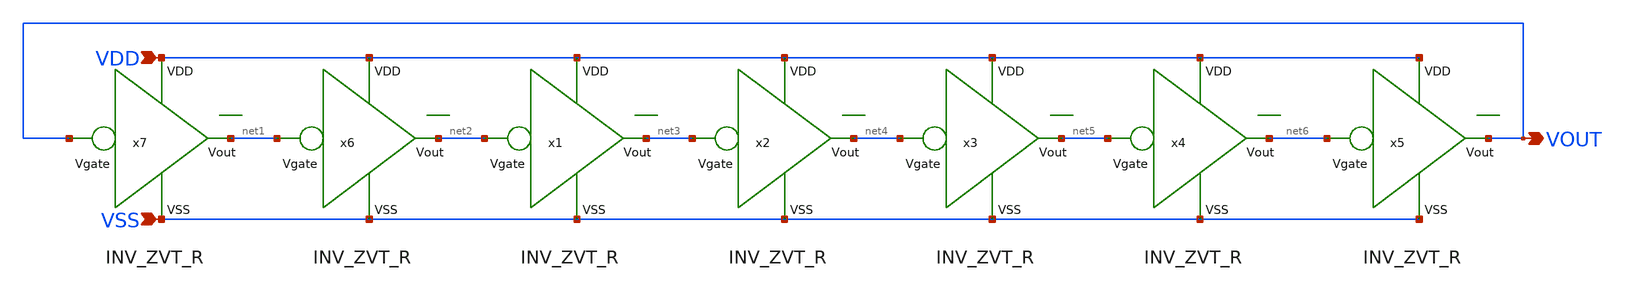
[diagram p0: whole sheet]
** sch_path: design/THESIS_EXP_RO_INVERTER_SKY130A/OSC_ZVT.sch
**.subckt OSC_ZVT VDD VSS VOUT
*.ipin VDD
*.ipin VSS
*.opin VOUT
x1 VDD net3 net2 VSS INV_ZVT_R
x2 VDD net4 net3 VSS INV_ZVT_R
x3 VDD net5 net4 VSS INV_ZVT_R
x4 VDD net6 net5 VSS INV_ZVT_R
x5 VDD VOUT net6 VSS INV_ZVT_R
x6 VDD net2 net1 VSS INV_ZVT_R
x7 VDD net1 VOUT VSS INV_ZVT_R
**.ends

* expanding   symbol:  THESIS_EXP_RO_INVERTER_SKY130A/INV_ZVT_R.sym # of pins=4
** sym_path: design/THESIS_EXP_RO_INVERTER_SKY130A/INV_ZVT_R.sym
** sch_path: design/THESIS_EXP_RO_INVERTER_SKY130A/INV_ZVT_R.sch
.subckt INV_ZVT_R VDD Vout Vgate VSS
*.ipin VDD
*.ipin VSS
*.ipin Vgate
*.opin Vout
R1 VDD Vout 50k m=1
x1 Vout Vgate VSS VSS JNW_LVT_ATR_20V_2x_30_5-5
.ends


* expanding   symbol:  JNW_ZVT_ATR_SKY130A/JNW_LVT_ATR_20V_2x_30_5-5.sym # of pins=4
** sym_path: design/JNW_ZVT_ATR_SKY130A/JNW_LVT_ATR_20V_2x_30_5-5.sym
** sch_path: design/JNW_ZVT_ATR_SKY130A/JNW_LVT_ATR_20V_2x_30_5-5.sch
.subckt JNW_LVT_ATR_20V_2x_30_5-5 D G S B
*.iopin D
*.iopin G
*.iopin S
*.iopin B
XM1 D G S B sky130_fd_pr__nfet_20v0_zvt W=30 L=5.5 m=2
.ends

.end
